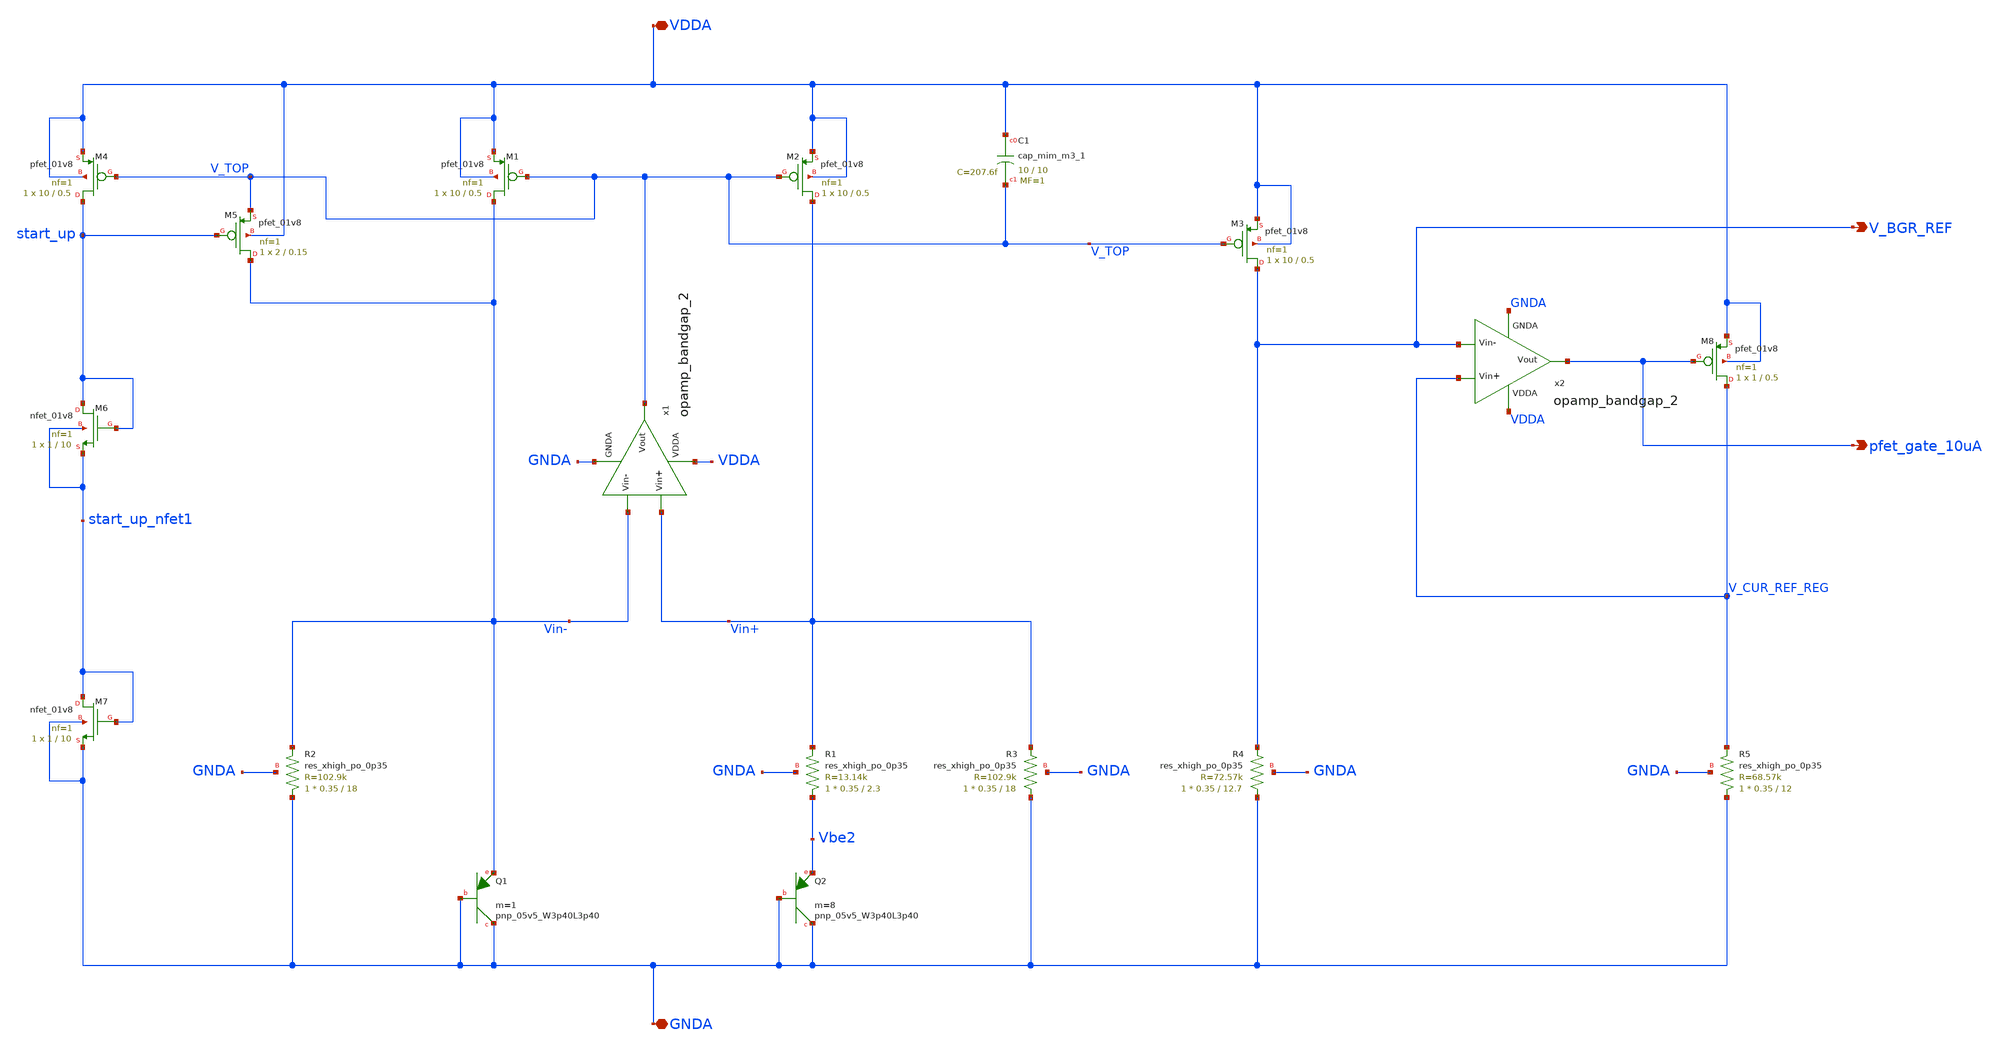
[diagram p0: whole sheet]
** sch_path: projects/opamp/xschem_ngspice/ref_volt_cur_gen.sch
**.subckt ref_volt_cur_gen pfet_gate_10uA GNDA V_BGR_REF VDDA
*.opin pfet_gate_10uA
*.iopin GNDA
*.opin V_BGR_REF
*.iopin VDDA
XM3 V_BGR_REF V_TOP VDDA VDDA sky130_fd_pr__pfet_01v8 L=0.5 W=10 nf=1 ad='int((nf+1)/2) * W/nf * 0.29'
+ as='int((nf+2)/2) * W/nf * 0.29' pd='2*int((nf+1)/2) * (W/nf + 0.29)' ps='2*int((nf+2)/2) * (W/nf + 0.29)'
+ nrd='0.29 / W' nrs='0.29 / W' sa=0 sb=0 sd=0 mult=1 m=1
XR4 GNDA V_BGR_REF GNDA sky130_fd_pr__res_xhigh_po_0p35 L=12.7 mult=1 m=1
XR5 GNDA V_CUR_REF_REG GNDA sky130_fd_pr__res_xhigh_po_0p35 L=12 mult=1 m=1
XM8 V_CUR_REF_REG pfet_gate_10uA VDDA VDDA sky130_fd_pr__pfet_01v8 L=0.5 W=1 nf=1 ad='int((nf+1)/2) * W/nf * 0.29'
+ as='int((nf+2)/2) * W/nf * 0.29' pd='2*int((nf+1)/2) * (W/nf + 0.29)' ps='2*int((nf+2)/2) * (W/nf + 0.29)'
+ nrd='0.29 / W' nrs='0.29 / W' sa=0 sb=0 sd=0 mult=1 m=1
x2 VDDA pfet_gate_10uA V_BGR_REF V_CUR_REF_REG GNDA opamp_bandgap_2
XC1 VDDA V_TOP sky130_fd_pr__cap_mim_m3_1 W=10 L=10 MF=1 m=1
XQ1 GNDA GNDA Vin- sky130_fd_pr__pnp_05v5_W3p40L3p40 m=1
XQ2 GNDA GNDA Vbe2 sky130_fd_pr__pnp_05v5_W3p40L3p40 m=8
XM1 Vin- V_TOP VDDA VDDA sky130_fd_pr__pfet_01v8 L=0.5 W=10 nf=1 ad='int((nf+1)/2) * W/nf * 0.29' as='int((nf+2)/2) * W/nf * 0.29'
+ pd='2*int((nf+1)/2) * (W/nf + 0.29)' ps='2*int((nf+2)/2) * (W/nf + 0.29)' nrd='0.29 / W' nrs='0.29 / W'
+ sa=0 sb=0 sd=0 mult=1 m=1
XM2 Vin+ V_TOP VDDA VDDA sky130_fd_pr__pfet_01v8 L=0.5 W=10 nf=1 ad='int((nf+1)/2) * W/nf * 0.29' as='int((nf+2)/2) * W/nf * 0.29'
+ pd='2*int((nf+1)/2) * (W/nf + 0.29)' ps='2*int((nf+2)/2) * (W/nf + 0.29)' nrd='0.29 / W' nrs='0.29 / W'
+ sa=0 sb=0 sd=0 mult=1 m=1
XR1 Vbe2 Vin+ GNDA sky130_fd_pr__res_xhigh_po_0p35 L=2.3 mult=1 m=1
XR3 GNDA Vin+ GNDA sky130_fd_pr__res_xhigh_po_0p35 L=18 mult=1 m=1
XR2 GNDA Vin- GNDA sky130_fd_pr__res_xhigh_po_0p35 L=18 mult=1 m=1
XM6 start_up start_up start_up_nfet1 start_up_nfet1 sky130_fd_pr__nfet_01v8 L=10 W=1 nf=1 ad='int((nf+1)/2) * W/nf * 0.29'
+ as='int((nf+2)/2) * W/nf * 0.29' pd='2*int((nf+1)/2) * (W/nf + 0.29)' ps='2*int((nf+2)/2) * (W/nf + 0.29)'
+ nrd='0.29 / W' nrs='0.29 / W' sa=0 sb=0 sd=0 mult=1 m=1
XM4 start_up V_TOP VDDA VDDA sky130_fd_pr__pfet_01v8 L=0.5 W=10 nf=1 ad='int((nf+1)/2) * W/nf * 0.29'
+ as='int((nf+2)/2) * W/nf * 0.29' pd='2*int((nf+1)/2) * (W/nf + 0.29)' ps='2*int((nf+2)/2) * (W/nf + 0.29)'
+ nrd='0.29 / W' nrs='0.29 / W' sa=0 sb=0 sd=0 mult=1 m=1
XM5 Vin- start_up V_TOP VDDA sky130_fd_pr__pfet_01v8 L=0.15 W=2 nf=1 ad='int((nf+1)/2) * W/nf * 0.29'
+ as='int((nf+2)/2) * W/nf * 0.29' pd='2*int((nf+1)/2) * (W/nf + 0.29)' ps='2*int((nf+2)/2) * (W/nf + 0.29)'
+ nrd='0.29 / W' nrs='0.29 / W' sa=0 sb=0 sd=0 mult=1 m=1
XM7 start_up_nfet1 start_up_nfet1 GNDA GNDA sky130_fd_pr__nfet_01v8 L=10 W=1 nf=1 ad='int((nf+1)/2) * W/nf * 0.29'
+ as='int((nf+2)/2) * W/nf * 0.29' pd='2*int((nf+1)/2) * (W/nf + 0.29)' ps='2*int((nf+2)/2) * (W/nf + 0.29)'
+ nrd='0.29 / W' nrs='0.29 / W' sa=0 sb=0 sd=0 mult=1 m=1
x1 VDDA V_TOP Vin- Vin+ GNDA opamp_bandgap_2
**.ends

* expanding   symbol:
*+  /foss/designs/my_design/projects/bandgapref/xschem_ngspice/new_files/opamp_bandgap_2.sym # of pins=5
** sym_path: projects/bandgapref/xschem_ngspice/new_files/opamp_bandgap_2.sym
** sch_path: projects/bandgapref/xschem_ngspice/new_files/opamp_bandgap_2.sch
.subckt opamp_bandgap_2 VDDA Vout Vin- Vin+ GNDA
*.ipin Vin+
*.opin Vout
*.ipin Vin-
*.ipin GNDA
*.ipin VDDA
XM1 V_p VDDA GNDA GNDA sky130_fd_pr__nfet_01v8 L=5 W=2.5 nf=1 ad='int((nf+1)/2) * W/nf * 0.29' as='int((nf+2)/2) * W/nf * 0.29'
+ pd='2*int((nf+1)/2) * (W/nf + 0.29)' ps='2*int((nf+2)/2) * (W/nf + 0.29)' nrd='0.29 / W' nrs='0.29 / W'
+ sa=0 sb=0 sd=0 mult=1 m=1
XM2 V_mirror Vin- V_p GNDA sky130_fd_pr__nfet_01v8 L=0.2 W=2.5 nf=1 ad='int((nf+1)/2) * W/nf * 0.29'
+ as='int((nf+2)/2) * W/nf * 0.29' pd='2*int((nf+1)/2) * (W/nf + 0.29)' ps='2*int((nf+2)/2) * (W/nf + 0.29)'
+ nrd='0.29 / W' nrs='0.29 / W' sa=0 sb=0 sd=0 mult=1 m=1
XM3 1st_Vout Vin+ V_p GNDA sky130_fd_pr__nfet_01v8 L=0.2 W=2.5 nf=1 ad='int((nf+1)/2) * W/nf * 0.29'
+ as='int((nf+2)/2) * W/nf * 0.29' pd='2*int((nf+1)/2) * (W/nf + 0.29)' ps='2*int((nf+2)/2) * (W/nf + 0.29)'
+ nrd='0.29 / W' nrs='0.29 / W' sa=0 sb=0 sd=0 mult=1 m=1
XM5 V_mirror V_mirror VDDA VDDA sky130_fd_pr__pfet_01v8 L=0.2 W=6 nf=2 ad='int((nf+1)/2) * W/nf * 0.29'
+ as='int((nf+2)/2) * W/nf * 0.29' pd='2*int((nf+1)/2) * (W/nf + 0.29)' ps='2*int((nf+2)/2) * (W/nf + 0.29)'
+ nrd='0.29 / W' nrs='0.29 / W' sa=0 sb=0 sd=0 mult=1 m=1
XM6 1st_Vout V_mirror VDDA VDDA sky130_fd_pr__pfet_01v8 L=0.2 W=6 nf=2 ad='int((nf+1)/2) * W/nf * 0.29'
+ as='int((nf+2)/2) * W/nf * 0.29' pd='2*int((nf+1)/2) * (W/nf + 0.29)' ps='2*int((nf+2)/2) * (W/nf + 0.29)'
+ nrd='0.29 / W' nrs='0.29 / W' sa=0 sb=0 sd=0 mult=1 m=1
XM4 Vout VDDA GNDA GNDA sky130_fd_pr__nfet_01v8 L=5 W=2.5 nf=1 ad='int((nf+1)/2) * W/nf * 0.29' as='int((nf+2)/2) * W/nf * 0.29'
+ pd='2*int((nf+1)/2) * (W/nf + 0.29)' ps='2*int((nf+2)/2) * (W/nf + 0.29)' nrd='0.29 / W' nrs='0.29 / W'
+ sa=0 sb=0 sd=0 mult=1 m=1
XM7 Vout 1st_Vout VDDA VDDA sky130_fd_pr__pfet_01v8 L=0.2 W=6 nf=2 ad='int((nf+1)/2) * W/nf * 0.29' as='int((nf+2)/2) * W/nf * 0.29'
+ pd='2*int((nf+1)/2) * (W/nf + 0.29)' ps='2*int((nf+2)/2) * (W/nf + 0.29)' nrd='0.29 / W' nrs='0.29 / W'
+ sa=0 sb=0 sd=0 mult=1 m=1
XC1 1st_Vout net1 sky130_fd_pr__cap_mim_m3_1 W=10 L=10 MF=1 m=1
XR1 Vout net1 GNDA sky130_fd_pr__res_xhigh_po_0p35 L=0.5 mult=1 m=1
.ends

.end
